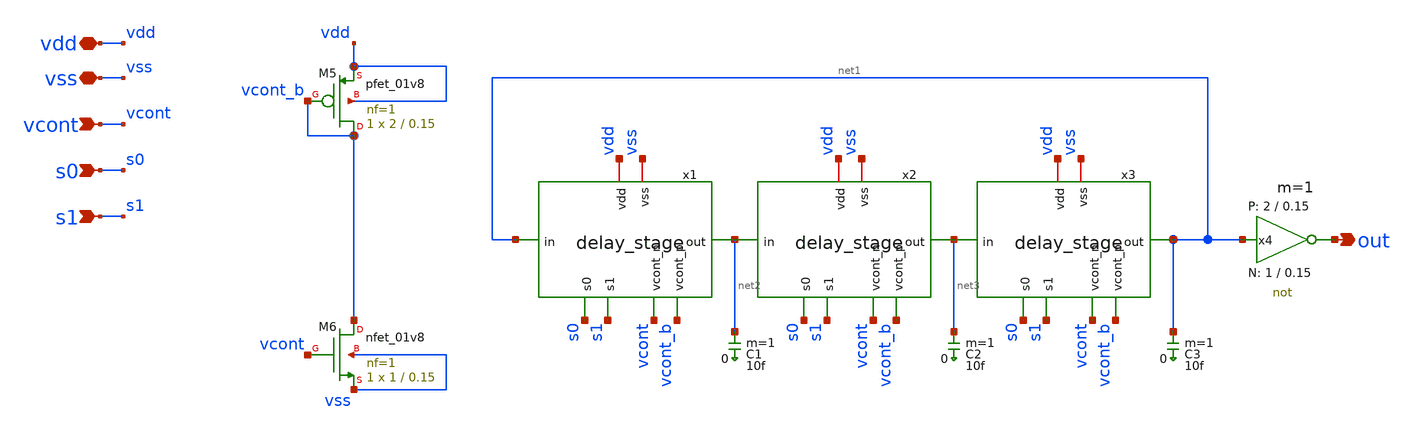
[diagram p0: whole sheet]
** sch_path: xschem/vco.sch
* StefanSchippers/xschem_sky130/sky130_tests/not.sch:
* Copyright 2021 Stefan Frederik Schippers
* Licensed under the Apache License, Version 2.0 (the "License");
**.subckt vco out vdd s0 s1 vcont vss
*.opin out
*.iopin vdd
*.ipin s0
*.ipin s1
*.ipin vcont
*.iopin vss
x1 vdd vcont_b s0 s1 net2 net1 vcont vss delay_stage
x2 vdd vcont_b s0 s1 net3 net2 vcont vss delay_stage
x3 vdd vcont_b s0 s1 net1 net3 vcont vss delay_stage
C1 net2 0 10f m=1
C2 net3 0 10f m=1
C3 net1 0 10f m=1
x4 out net1 vdd vss not W_N=1 L_N=0.15 W_P=2 L_P=0.15 m=1
XM5 vcont_b vcont_b vdd vdd sky130_fd_pr__pfet_01v8 L=0.15 W=2 nf=1 ad='int((nf+1)/2) * W/nf * 0.29'
+ as='int((nf+2)/2) * W/nf * 0.29' pd='2*int((nf+1)/2) * (W/nf + 0.29)' ps='2*int((nf+2)/2) * (W/nf + 0.29)'
+ nrd='0.29 / W' nrs='0.29 / W' sa=0 sb=0 sd=0 mult=1 m=1
XM6 vcont_b vcont vss vss sky130_fd_pr__nfet_01v8 L=0.15 W=1 nf=1 ad='int((nf+1)/2) * W/nf * 0.29' as='int((nf+2)/2) * W/nf * 0.29'
+ pd='2*int((nf+1)/2) * (W/nf + 0.29)' ps='2*int((nf+2)/2) * (W/nf + 0.29)' nrd='0.29 / W' nrs='0.29 / W'
+ sa=0 sb=0 sd=0 mult=1 m=1
**.ends

* expanding   symbol:  delay_stage.sym # of pins=8
** sym_path: xschem/delay_stage.sym
** sch_path: xschem/delay_stage.sch
.subckt delay_stage vdd vcont_p s0 s1 out in vcont_n vss
*.ipin in
*.opin out
*.iopin vdd
*.ipin vcont_n
*.ipin vcont_p
*.ipin s0
*.ipin s1
*.iopin vss
XM3 out in net2 vss sky130_fd_pr__nfet_01v8 L=0.15 W=1 nf=1 ad='int((nf+1)/2) * W/nf * 0.29' as='int((nf+2)/2) * W/nf * 0.29'
+ pd='2*int((nf+1)/2) * (W/nf + 0.29)' ps='2*int((nf+2)/2) * (W/nf + 0.29)' nrd='0.29 / W' nrs='0.29 / W'
+ sa=0 sb=0 sd=0 mult=1 m=1
XM2 out in net1 vdd sky130_fd_pr__pfet_01v8 L=0.15 W=2 nf=1 ad='int((nf+1)/2) * W/nf * 0.29' as='int((nf+2)/2) * W/nf * 0.29'
+ pd='2*int((nf+1)/2) * (W/nf + 0.29)' ps='2*int((nf+2)/2) * (W/nf + 0.29)' nrd='0.29 / W' nrs='0.29 / W'
+ sa=0 sb=0 sd=0 mult=1 m=1
XM1 net1 vcont_p vdd vdd sky130_fd_pr__pfet_01v8 L=0.15 W=2 nf=1 ad='int((nf+1)/2) * W/nf * 0.29' as='int((nf+2)/2) * W/nf * 0.29'
+ pd='2*int((nf+1)/2) * (W/nf + 0.29)' ps='2*int((nf+2)/2) * (W/nf + 0.29)' nrd='0.29 / W' nrs='0.29 / W'
+ sa=0 sb=0 sd=0 mult=1 m=1
XM4 net2 vcont_n vss vss sky130_fd_pr__nfet_01v8 L=0.15 W=1 nf=1 ad='int((nf+1)/2) * W/nf * 0.29' as='int((nf+2)/2) * W/nf * 0.29'
+ pd='2*int((nf+1)/2) * (W/nf + 0.29)' ps='2*int((nf+2)/2) * (W/nf + 0.29)' nrd='0.29 / W' nrs='0.29 / W'
+ sa=0 sb=0 sd=0 mult=1 m=1
XC2 vss net3 sky130_fd_pr__cap_mim_m3_1 W=2.1 L=2.1 MF=1 m=1
XC1 vss net4 sky130_fd_pr__cap_mim_m3_1 W=2.1 L=4.2 MF=1 m=1
XM5 out s0 net4 vss sky130_fd_pr__nfet_01v8 L=0.15 W=1 nf=1 ad='int((nf+1)/2) * W/nf * 0.29' as='int((nf+2)/2) * W/nf * 0.29'
+ pd='2*int((nf+1)/2) * (W/nf + 0.29)' ps='2*int((nf+2)/2) * (W/nf + 0.29)' nrd='0.29 / W' nrs='0.29 / W'
+ sa=0 sb=0 sd=0 mult=1 m=1
XM6 out s1 net3 vss sky130_fd_pr__nfet_01v8 L=0.15 W=1 nf=1 ad='int((nf+1)/2) * W/nf * 0.29' as='int((nf+2)/2) * W/nf * 0.29'
+ pd='2*int((nf+1)/2) * (W/nf + 0.29)' ps='2*int((nf+2)/2) * (W/nf + 0.29)' nrd='0.29 / W' nrs='0.29 / W'
+ sa=0 sb=0 sd=0 mult=1 m=1
.ends


* expanding   symbol:  not.sym # of pins=2
** sym_path: not.sym
** sch_path: not.sch
.subckt not y a VCCPIN VSSPIN     W_N=1 L_N=0.15 W_P=2 L_P=0.15
*.opin y
*.ipin a
XM1 DN a VSSPIN VSSPIN sky130_fd_pr__nfet_01v8 L=L_N W=W_N nf=1 ad='int((1 + 1)/2) * W_N / 1 * 0.29'
+ as='int((1 + 2)/2) * W_N / 1 * 0.29' pd='2*int((1 + 1)/2) * (W_N / 1 + 0.29)' ps='2*int((1 + 2)/2) * (W_N / 1 + 0.29)'
+ nrd='0.29 / W_N ' nrs='0.29 / W_N ' sa=0 sb=0 sd=0 mult=1 m=1
XM2 DP a VCCPIN VCCPIN sky130_fd_pr__pfet_01v8 L=L_P W=W_P nf=1 ad='int((nf+1)/2) * W/nf * 0.29' as='int((nf+2)/2) * W/nf * 0.29'
+ pd='2*int((nf+1)/2) * (W/nf + 0.29)' ps='2*int((nf+2)/2) * (W/nf + 0.29)' nrd='0.29 / W' nrs='0.29 / W'
+ sa=0 sb=0 sd=0 mult=1 m=1
Vmeas DP y 0
.save i(vmeas)
Vmeas1 y DN 0
.save i(vmeas1)
.save v(dp)
.save v(dn)
.ends

.end
